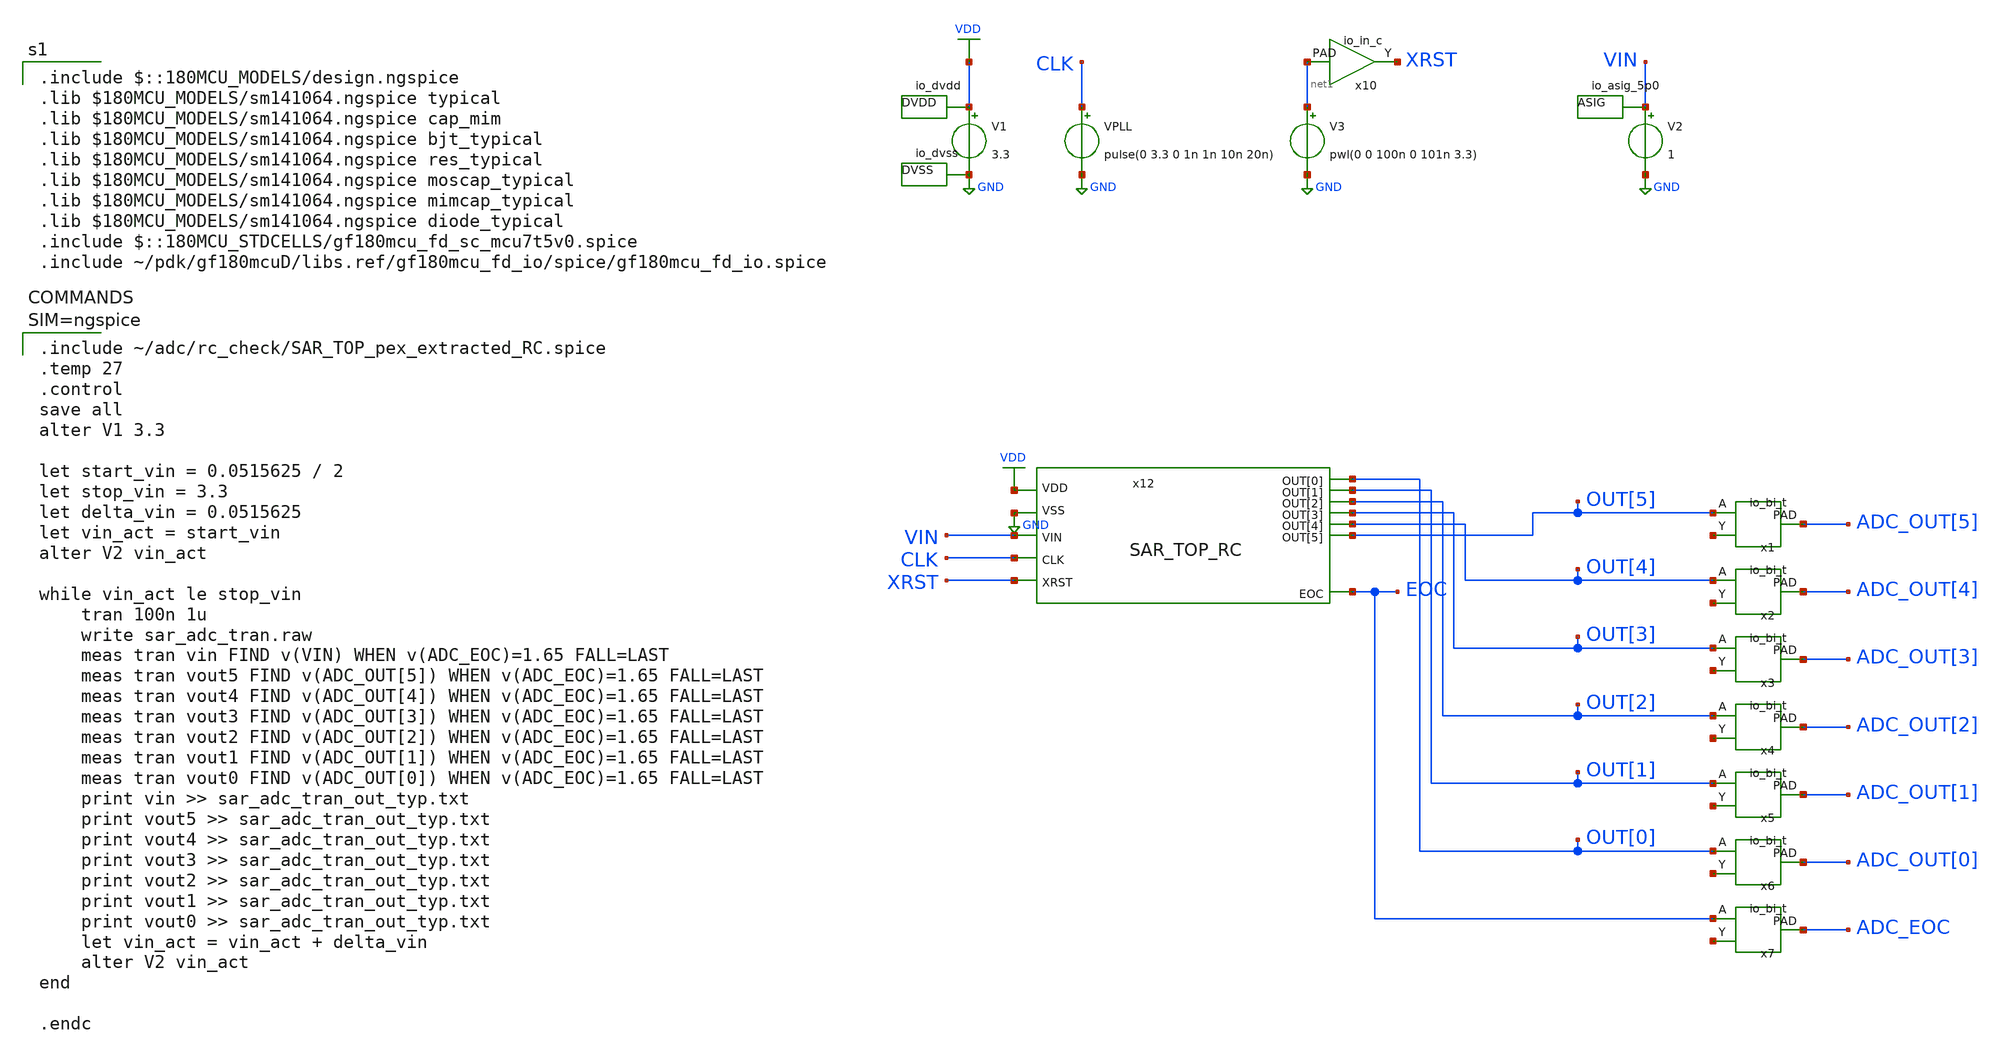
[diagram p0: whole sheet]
** sch_path: submit_version/xschem/tran_sar_adc_pex.sch
**.subckt tran_sar_adc_pex
V1 VDD GND 3.3
VPLL CLK GND pulse(0 3.3 0 1n 1n 10n 20n)
V3 net1 GND pwl(0 0 100n 0 101n 3.3)
V2 VIN GND 1
x1 OUT[5] 0 VDD 0 0 VDD ADC_OUT[5] 0 VDD VDD 0 0 VDD 0 net2 gf180mcu_fd_io__bi_t
x8 VDD DVSS 0 gf180mcu_fd_io__dvdd
x9 DVDD GND VDD gf180mcu_fd_io__dvss
x10 DVDD DVSS net1 0 0 VDD 0 XRST gf180mcu_fd_io__in_c
x11 VIN DVDD DVSS VDD 0 gf180mcu_fd_io__asig_5p0
x2 OUT[4] 0 VDD 0 0 VDD ADC_OUT[4] 0 VDD VDD 0 0 VDD 0 net3 gf180mcu_fd_io__bi_t
x3 OUT[3] 0 VDD 0 0 VDD ADC_OUT[3] 0 VDD VDD 0 0 VDD 0 net4 gf180mcu_fd_io__bi_t
x4 OUT[2] 0 VDD 0 0 VDD ADC_OUT[2] 0 VDD VDD 0 0 VDD 0 net5 gf180mcu_fd_io__bi_t
x5 OUT[1] 0 VDD 0 0 VDD ADC_OUT[1] 0 VDD VDD 0 0 VDD 0 net6 gf180mcu_fd_io__bi_t
x6 OUT[0] 0 VDD 0 0 VDD ADC_OUT[0] 0 VDD VDD 0 0 VDD 0 net7 gf180mcu_fd_io__bi_t
x7 EOC 0 VDD 0 0 VDD ADC_EOC 0 VDD VDD 0 0 VDD 0 net8 gf180mcu_fd_io__bi_t
x12 VIN GND VDD XRST CLK OUT[1] OUT[0] OUT[3] OUT[2] OUT[5] OUT[4] EOC SAR_TOP
**** begin user architecture code


.include ~/adc/rc_check/SAR_TOP_pex_extracted_RC.spice
.temp 27
.control
save all
alter V1 3.3

let start_vin = 0.0515625 / 2
let stop_vin = 3.3
let delta_vin = 0.0515625
let vin_act = start_vin
alter V2 vin_act

while vin_act le stop_vin
	tran 100n 1u
	write sar_adc_tran.raw
	meas tran vin FIND v(VIN) WHEN v(ADC_EOC)=1.65 FALL=LAST
	meas tran vout5 FIND v(ADC_OUT[5]) WHEN v(ADC_EOC)=1.65 FALL=LAST
	meas tran vout4 FIND v(ADC_OUT[4]) WHEN v(ADC_EOC)=1.65 FALL=LAST
	meas tran vout3 FIND v(ADC_OUT[3]) WHEN v(ADC_EOC)=1.65 FALL=LAST
	meas tran vout2 FIND v(ADC_OUT[2]) WHEN v(ADC_EOC)=1.65 FALL=LAST
	meas tran vout1 FIND v(ADC_OUT[1]) WHEN v(ADC_EOC)=1.65 FALL=LAST
	meas tran vout0 FIND v(ADC_OUT[0]) WHEN v(ADC_EOC)=1.65 FALL=LAST
	print vin >> sar_adc_tran_out_typ.txt
	print vout5 >> sar_adc_tran_out_typ.txt
	print vout4 >> sar_adc_tran_out_typ.txt
	print vout3 >> sar_adc_tran_out_typ.txt
	print vout2 >> sar_adc_tran_out_typ.txt
	print vout1 >> sar_adc_tran_out_typ.txt
	print vout0 >> sar_adc_tran_out_typ.txt
	let vin_act = vin_act + delta_vin
	alter V2 vin_act
end

.endc



 .include $::180MCU_MODELS/design.ngspice
.lib $180MCU_MODELS/sm141064.ngspice typical
.lib $180MCU_MODELS/sm141064.ngspice cap_mim
.lib $180MCU_MODELS/sm141064.ngspice bjt_typical
.lib $180MCU_MODELS/sm141064.ngspice res_typical
.lib $180MCU_MODELS/sm141064.ngspice moscap_typical
.lib $180MCU_MODELS/sm141064.ngspice mimcap_typical
.lib $180MCU_MODELS/sm141064.ngspice diode_typical
.include $::180MCU_STDCELLS/gf180mcu_fd_sc_mcu7t5v0.spice
.include ~/pdk/gf180mcuD/libs.ref/gf180mcu_fd_io/spice/gf180mcu_fd_io.spice
**** end user architecture code
**.ends
.GLOBAL GND
.GLOBAL VDD
.end
